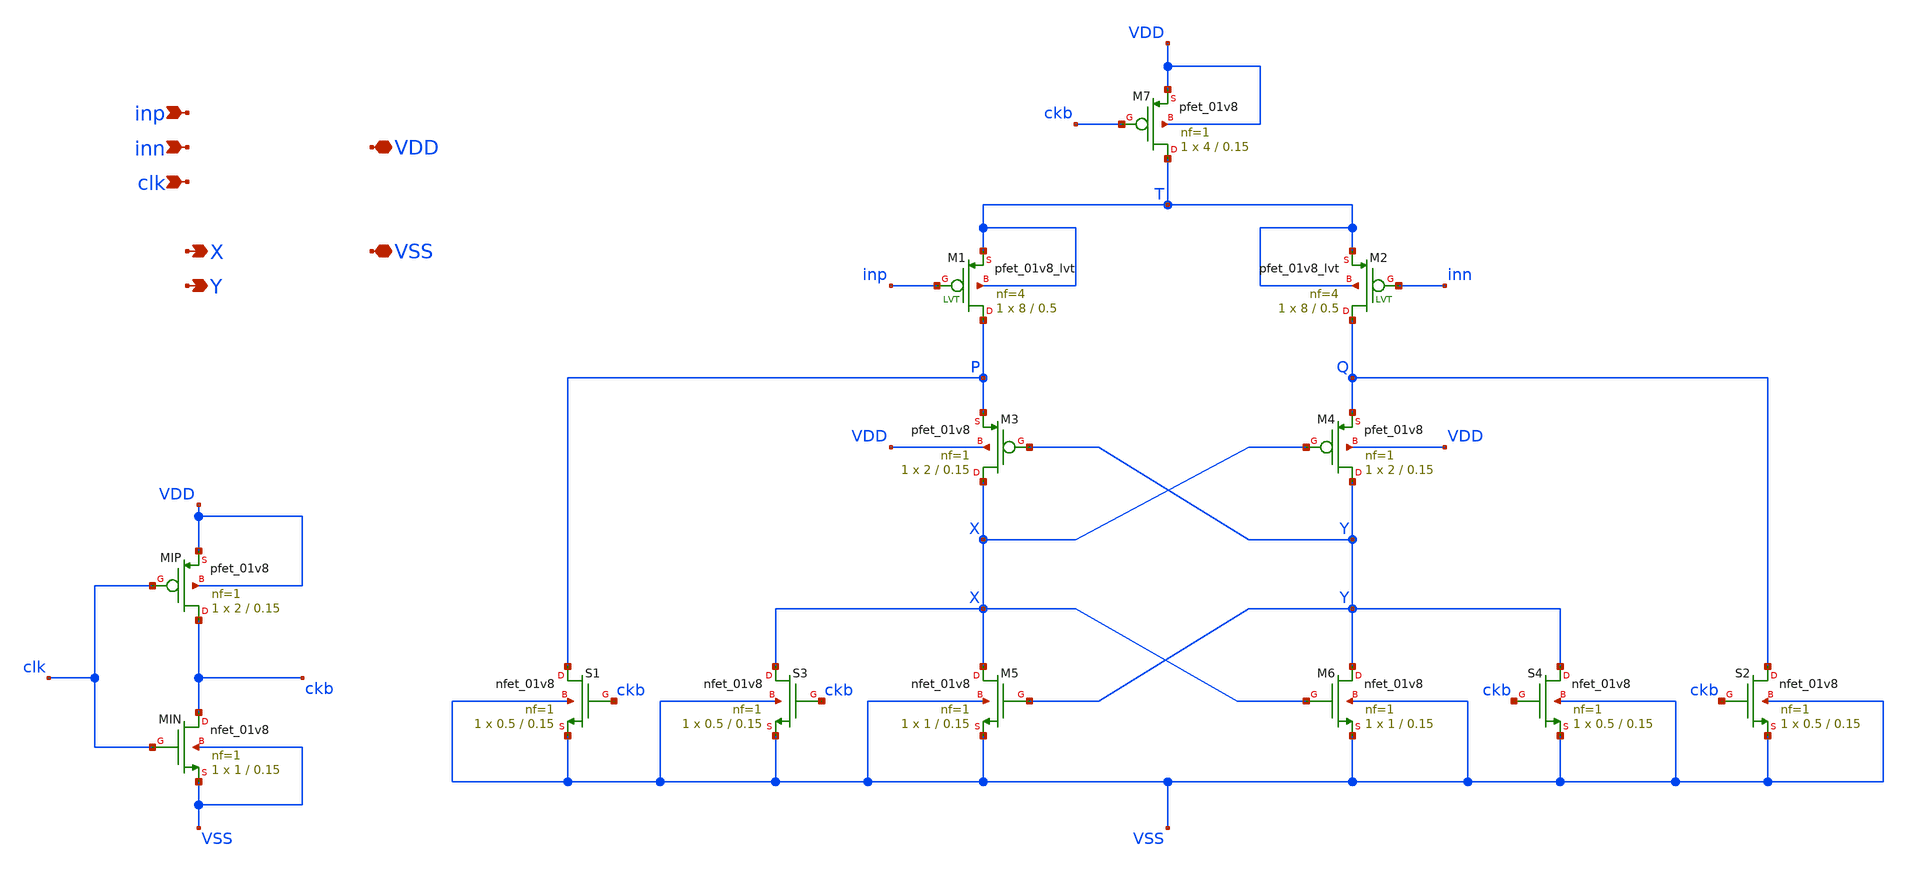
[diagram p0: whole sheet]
** sch_path: xschem/comparator_sa.sch
**.subckt comparator_sa inp inn clk X Y VDD VSS
*.ipin inp
*.ipin inn
*.ipin clk
*.opin X
*.opin Y
*.iopin VDD
*.iopin VSS
XM7 T ckb VDD VDD sky130_fd_pr__pfet_01v8 L=0.15 W=4 nf=1 ad='int((1 + 1)/2) * 4 / 1 * 0.29' as='int((1 + 2)/2) * 4 / 1 * 0.29'
+ pd='2*int((1 + 1)/2) * (4 / 1 + 0.29)' ps='2*int((1 + 2)/2) * (4 / 1 + 0.29)' nrd='0.29 / 4 ' nrs='0.29 / 4 '
+ sa=0 sb=0 sd=0 mult=1 m=1
XM1 P inp T T sky130_fd_pr__pfet_01v8_lvt L=0.5 W=8 nf=4 ad='int((4 + 1)/2) * 8 / 4 * 0.29' as='int((4 + 2)/2) * 8 / 4 * 0.29'
+ pd='2*int((4 + 1)/2) * (8 / 4 + 0.29)' ps='2*int((4 + 2)/2) * (8 / 4 + 0.29)' nrd='0.29 / 8 ' nrs='0.29 / 8 '
+ sa=0 sb=0 sd=0 mult=1 m=1
XM2 Q inn T T sky130_fd_pr__pfet_01v8_lvt L=0.5 W=8 nf=4 ad='int((4 + 1)/2) * 8 / 4 * 0.29' as='int((4 + 2)/2) * 8 / 4 * 0.29'
+ pd='2*int((4 + 1)/2) * (8 / 4 + 0.29)' ps='2*int((4 + 2)/2) * (8 / 4 + 0.29)' nrd='0.29 / 8 ' nrs='0.29 / 8 '
+ sa=0 sb=0 sd=0 mult=1 m=1
XM3 X Y P VDD sky130_fd_pr__pfet_01v8 L=0.15 W=2 nf=1 ad='int((1 + 1)/2) * 2 / 1 * 0.29' as='int((1 + 2)/2) * 2 / 1 * 0.29'
+ pd='2*int((1 + 1)/2) * (2 / 1 + 0.29)' ps='2*int((1 + 2)/2) * (2 / 1 + 0.29)' nrd='0.29 / 2 ' nrs='0.29 / 2 '
+ sa=0 sb=0 sd=0 mult=1 m=1
XM4 Y X Q VDD sky130_fd_pr__pfet_01v8 L=0.15 W=2 nf=1 ad='int((1 + 1)/2) * 2 / 1 * 0.29' as='int((1 + 2)/2) * 2 / 1 * 0.29'
+ pd='2*int((1 + 1)/2) * (2 / 1 + 0.29)' ps='2*int((1 + 2)/2) * (2 / 1 + 0.29)' nrd='0.29 / 2 ' nrs='0.29 / 2 '
+ sa=0 sb=0 sd=0 mult=1 m=1
XM6 Y X VSS VSS sky130_fd_pr__nfet_01v8 L=0.15 W=1 nf=1 ad='int((1 + 1)/2) * 1 / 1 * 0.29' as='int((1 + 2)/2) * 1 / 1 * 0.29'
+ pd='2*int((1 + 1)/2) * (1 / 1 + 0.29)' ps='2*int((1 + 2)/2) * (1 / 1 + 0.29)' nrd='0.29 / 1 ' nrs='0.29 / 1 '
+ sa=0 sb=0 sd=0 mult=1 m=1
XM5 X Y VSS VSS sky130_fd_pr__nfet_01v8 L=0.15 W=1 nf=1 ad='int((1 + 1)/2) * 1 / 1 * 0.29' as='int((1 + 2)/2) * 1 / 1 * 0.29'
+ pd='2*int((1 + 1)/2) * (1 / 1 + 0.29)' ps='2*int((1 + 2)/2) * (1 / 1 + 0.29)' nrd='0.29 / 1 ' nrs='0.29 / 1 '
+ sa=0 sb=0 sd=0 mult=1 m=1
XS4 Y ckb VSS VSS sky130_fd_pr__nfet_01v8 L=0.15 W=0.5 nf=1 ad='int((1 + 1)/2) * 0.5 / 1 * 0.29' as='int((1 + 2)/2) * 0.5 / 1 * 0.29'
+ pd='2*int((1 + 1)/2) * (0.5 / 1 + 0.29)' ps='2*int((1 + 2)/2) * (0.5 / 1 + 0.29)' nrd='0.29 / 0.5 ' nrs='0.29 / 0.5 '
+ sa=0 sb=0 sd=0 mult=1 m=1
XS2 Q ckb VSS VSS sky130_fd_pr__nfet_01v8 L=0.15 W=0.5 nf=1 ad='int((1 + 1)/2) * 0.5 / 1 * 0.29' as='int((1 + 2)/2) * 0.5 / 1 * 0.29'
+ pd='2*int((1 + 1)/2) * (0.5 / 1 + 0.29)' ps='2*int((1 + 2)/2) * (0.5 / 1 + 0.29)' nrd='0.29 / 0.5 ' nrs='0.29 / 0.5 '
+ sa=0 sb=0 sd=0 mult=1 m=1
XS3 X ckb VSS VSS sky130_fd_pr__nfet_01v8 L=0.15 W=0.5 nf=1 ad='int((1 + 1)/2) * 0.5 / 1 * 0.29' as='int((1 + 2)/2) * 0.5 / 1 * 0.29'
+ pd='2*int((1 + 1)/2) * (0.5 / 1 + 0.29)' ps='2*int((1 + 2)/2) * (0.5 / 1 + 0.29)' nrd='0.29 / 0.5 ' nrs='0.29 / 0.5 '
+ sa=0 sb=0 sd=0 mult=1 m=1
XS1 P ckb VSS VSS sky130_fd_pr__nfet_01v8 L=0.15 W=0.5 nf=1 ad='int((1 + 1)/2) * 0.5 / 1 * 0.29' as='int((1 + 2)/2) * 0.5 / 1 * 0.29'
+ pd='2*int((1 + 1)/2) * (0.5 / 1 + 0.29)' ps='2*int((1 + 2)/2) * (0.5 / 1 + 0.29)' nrd='0.29 / 0.5 ' nrs='0.29 / 0.5 '
+ sa=0 sb=0 sd=0 mult=1 m=1
XMIN ckb clk VSS VSS sky130_fd_pr__nfet_01v8 L=0.15 W=1 nf=1 ad='int((1 + 1)/2) * 1 / 1 * 0.29' as='int((1 + 2)/2) * 1 / 1 * 0.29'
+ pd='2*int((1 + 1)/2) * (1 / 1 + 0.29)' ps='2*int((1 + 2)/2) * (1 / 1 + 0.29)' nrd='0.29 / 1 ' nrs='0.29 / 1 '
+ sa=0 sb=0 sd=0 mult=1 m=1
XMIP ckb clk VDD VDD sky130_fd_pr__pfet_01v8 L=0.15 W=2 nf=1 ad='int((1 + 1)/2) * 2 / 1 * 0.29' as='int((1 + 2)/2) * 2 / 1 * 0.29'
+ pd='2*int((1 + 1)/2) * (2 / 1 + 0.29)' ps='2*int((1 + 2)/2) * (2 / 1 + 0.29)' nrd='0.29 / 2 ' nrs='0.29 / 2 '
+ sa=0 sb=0 sd=0 mult=1 m=1
**.ends
.end
